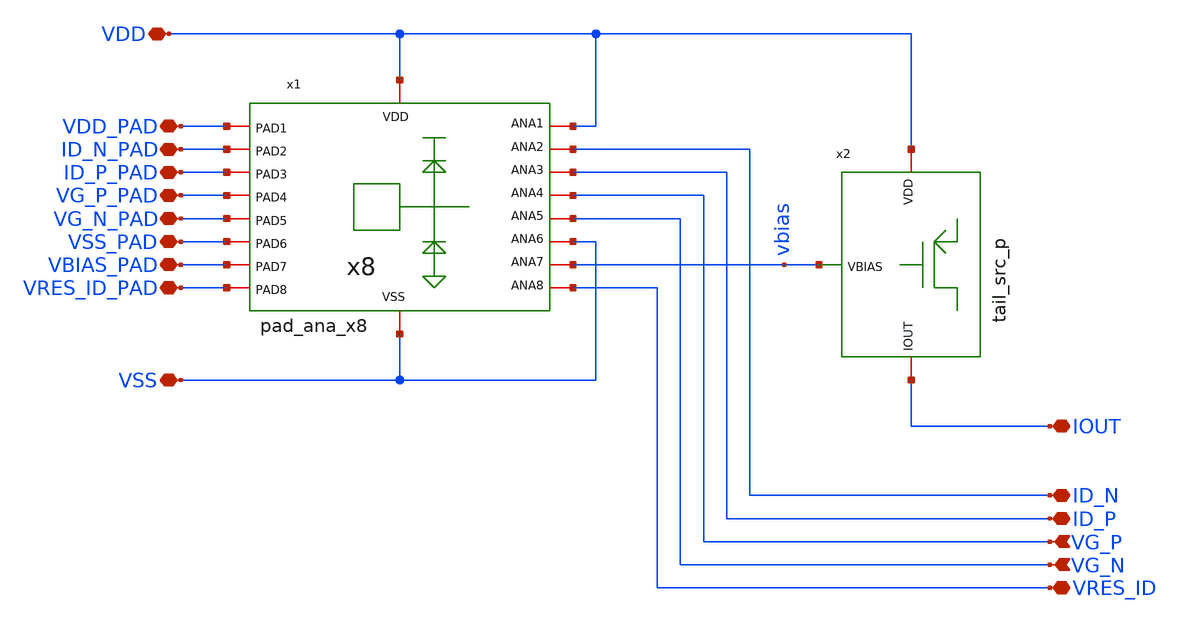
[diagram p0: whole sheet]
** sch_path: xschem/testcells/tb_pmos.sch
**.subckt tb_pmos VDD_PAD ID_N_PAD ID_P_PAD VG_P_PAD VG_N_PAD VSS_PAD VBIAS_PAD VRES_ID_PAD VSS IOUT
*+ VRES_ID ID_N ID_P VG_P VG_N VDD
*.iopin VDD_PAD
*.iopin ID_N_PAD
*.iopin ID_P_PAD
*.iopin VG_P_PAD
*.iopin VG_N_PAD
*.iopin VSS_PAD
*.iopin VBIAS_PAD
*.iopin VRES_ID_PAD
*.iopin VSS
*.iopin IOUT
*.iopin VRES_ID
*.iopin ID_N
*.iopin ID_P
*.ipin VG_P
*.ipin VG_N
*.iopin VDD
x1 VSS_PAD VDD_PAD VG_P_PAD VG_N_PAD ID_N_PAD ID_P_PAD VBIAS_PAD VRES_ID_PAD VDD VSS VG_N VG_P
+ VRES_ID ID_P vbias VSS ID_N VDD pad_ana_x8
x2 VDD vbias IOUT tail_src_p
**.ends
.end
